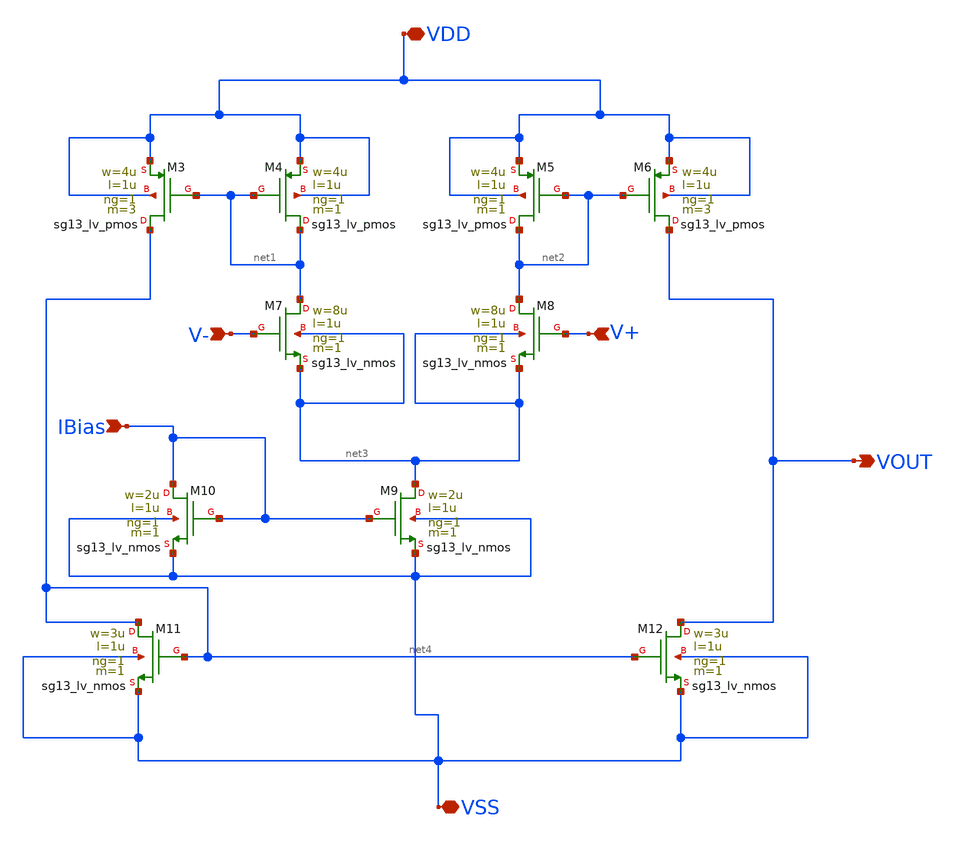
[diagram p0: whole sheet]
** sch_path: BPF/CurrentMirror-OTA.sch
**.subckt CurrentMirror-OTA VDD VSS V- VOUT V+ IBias
*.iopin VDD
*.iopin VSS
*.ipin V-
*.opin VOUT
*.ipin V+
*.ipin IBias
XM4 net1 net1 VDD VDD sg13_lv_pmos w=4u l=1u ng=1 m=1 mm_ok=1
XM3 net4 net1 VDD VDD sg13_lv_pmos w=4u l=1u ng=1 m=3 mm_ok=1
XM5 net2 net2 VDD VDD sg13_lv_pmos w=4u l=1u ng=1 m=1 mm_ok=1
XM6 VOUT net2 VDD VDD sg13_lv_pmos w=4u l=1u ng=1 m=3 mm_ok=1
XM7 net1 V- net3 net3 sg13_lv_nmos w=8u l=1u ng=1 m=1 mm_ok=1
XM8 net2 V+ net3 net3 sg13_lv_nmos w=8u l=1u ng=1 m=1 mm_ok=1
XM9 net3 IBias VSS VSS sg13_lv_nmos w=2u l=1u ng=1 m=1 mm_ok=1
XM10 IBias IBias VSS VSS sg13_lv_nmos w=2u l=1u ng=1 m=1 mm_ok=1
XM11 net4 net4 VSS VSS sg13_lv_nmos w=3u l=1u ng=1 m=1 mm_ok=1
XM12 VOUT net4 VSS VSS sg13_lv_nmos w=3u l=1u ng=1 m=1 mm_ok=1
**.ends
.end
